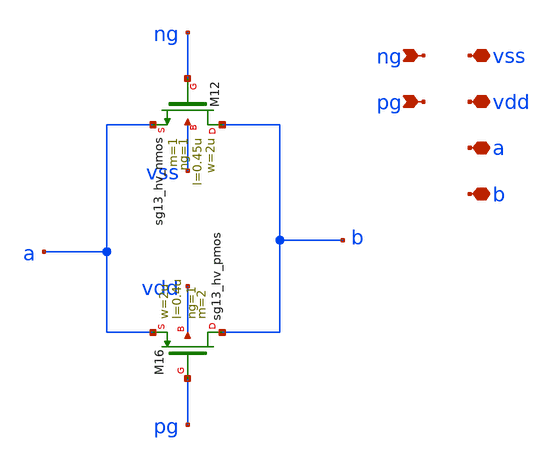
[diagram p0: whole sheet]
** sch_path: circuit_files/sar_adc_test/xschem/tg.sch
**.subckt tg ng vdd pg a b vss
*.ipin ng
*.iopin vdd
*.ipin pg
*.iopin a
*.iopin b
*.iopin vss
XM12 b ng a vss sg13_hv_nmos w=2u l=0.45u ng=1 m=1 mm_ok=1
XM16 b pg a vdd sg13_hv_pmos w=2u l=0.4u ng=1 m=2 mm_ok=1
**.ends
.end
